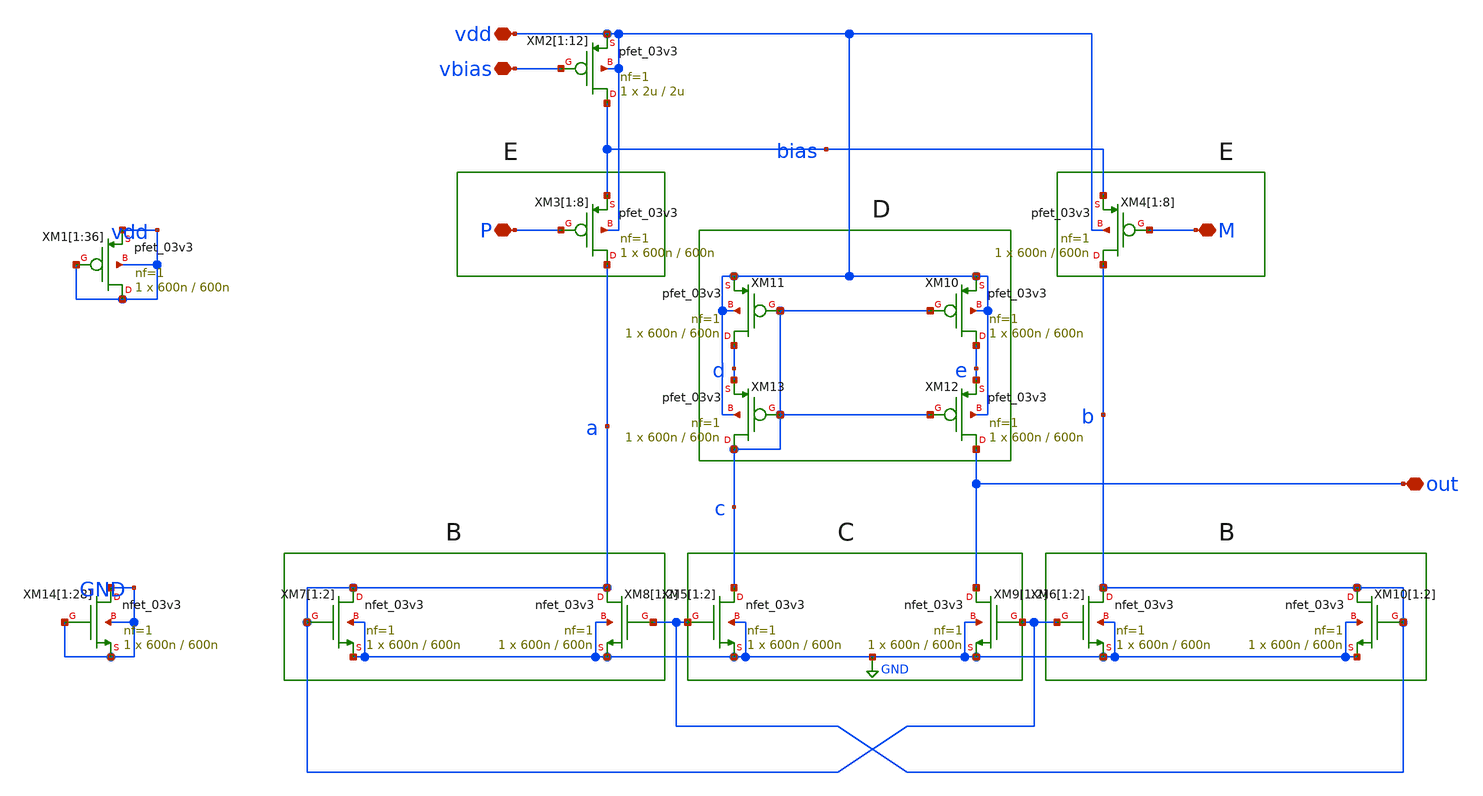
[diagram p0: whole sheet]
** sch_path: Clock_Reference/symbols_clock/comparatornew.sch
**.subckt comparatornew out M P vbias vdd
*.iopin out
*.iopin M
*.iopin P
*.iopin vbias
*.iopin vdd
XM2[1] bias vbias vdd vdd pfet_03v3 L=2u W=2u nf=1 ad='int((nf+1)/2) * W/nf * 0.18u' as='int((nf+2)/2) * W/nf * 0.18u'
+ pd='2*int((nf+1)/2) * (W/nf + 0.18u)' ps='2*int((nf+2)/2) * (W/nf + 0.18u)' nrd='0.18u / W' nrs='0.18u / W'
+ sa=0 sb=0 sd=0 m=1
XM2[2] bias vbias vdd vdd pfet_03v3 L=2u W=2u nf=1 ad='int((nf+1)/2) * W/nf * 0.18u' as='int((nf+2)/2) * W/nf * 0.18u'
+ pd='2*int((nf+1)/2) * (W/nf + 0.18u)' ps='2*int((nf+2)/2) * (W/nf + 0.18u)' nrd='0.18u / W' nrs='0.18u / W'
+ sa=0 sb=0 sd=0 m=1
XM2[3] bias vbias vdd vdd pfet_03v3 L=2u W=2u nf=1 ad='int((nf+1)/2) * W/nf * 0.18u' as='int((nf+2)/2) * W/nf * 0.18u'
+ pd='2*int((nf+1)/2) * (W/nf + 0.18u)' ps='2*int((nf+2)/2) * (W/nf + 0.18u)' nrd='0.18u / W' nrs='0.18u / W'
+ sa=0 sb=0 sd=0 m=1
XM2[4] bias vbias vdd vdd pfet_03v3 L=2u W=2u nf=1 ad='int((nf+1)/2) * W/nf * 0.18u' as='int((nf+2)/2) * W/nf * 0.18u'
+ pd='2*int((nf+1)/2) * (W/nf + 0.18u)' ps='2*int((nf+2)/2) * (W/nf + 0.18u)' nrd='0.18u / W' nrs='0.18u / W'
+ sa=0 sb=0 sd=0 m=1
XM2[5] bias vbias vdd vdd pfet_03v3 L=2u W=2u nf=1 ad='int((nf+1)/2) * W/nf * 0.18u' as='int((nf+2)/2) * W/nf * 0.18u'
+ pd='2*int((nf+1)/2) * (W/nf + 0.18u)' ps='2*int((nf+2)/2) * (W/nf + 0.18u)' nrd='0.18u / W' nrs='0.18u / W'
+ sa=0 sb=0 sd=0 m=1
XM2[6] bias vbias vdd vdd pfet_03v3 L=2u W=2u nf=1 ad='int((nf+1)/2) * W/nf * 0.18u' as='int((nf+2)/2) * W/nf * 0.18u'
+ pd='2*int((nf+1)/2) * (W/nf + 0.18u)' ps='2*int((nf+2)/2) * (W/nf + 0.18u)' nrd='0.18u / W' nrs='0.18u / W'
+ sa=0 sb=0 sd=0 m=1
XM2[7] bias vbias vdd vdd pfet_03v3 L=2u W=2u nf=1 ad='int((nf+1)/2) * W/nf * 0.18u' as='int((nf+2)/2) * W/nf * 0.18u'
+ pd='2*int((nf+1)/2) * (W/nf + 0.18u)' ps='2*int((nf+2)/2) * (W/nf + 0.18u)' nrd='0.18u / W' nrs='0.18u / W'
+ sa=0 sb=0 sd=0 m=1
XM2[8] bias vbias vdd vdd pfet_03v3 L=2u W=2u nf=1 ad='int((nf+1)/2) * W/nf * 0.18u' as='int((nf+2)/2) * W/nf * 0.18u'
+ pd='2*int((nf+1)/2) * (W/nf + 0.18u)' ps='2*int((nf+2)/2) * (W/nf + 0.18u)' nrd='0.18u / W' nrs='0.18u / W'
+ sa=0 sb=0 sd=0 m=1
XM2[9] bias vbias vdd vdd pfet_03v3 L=2u W=2u nf=1 ad='int((nf+1)/2) * W/nf * 0.18u' as='int((nf+2)/2) * W/nf * 0.18u'
+ pd='2*int((nf+1)/2) * (W/nf + 0.18u)' ps='2*int((nf+2)/2) * (W/nf + 0.18u)' nrd='0.18u / W' nrs='0.18u / W'
+ sa=0 sb=0 sd=0 m=1
XM2[10] bias vbias vdd vdd pfet_03v3 L=2u W=2u nf=1 ad='int((nf+1)/2) * W/nf * 0.18u' as='int((nf+2)/2) * W/nf * 0.18u'
+ pd='2*int((nf+1)/2) * (W/nf + 0.18u)' ps='2*int((nf+2)/2) * (W/nf + 0.18u)' nrd='0.18u / W' nrs='0.18u / W'
+ sa=0 sb=0 sd=0 m=1
XM2[11] bias vbias vdd vdd pfet_03v3 L=2u W=2u nf=1 ad='int((nf+1)/2) * W/nf * 0.18u' as='int((nf+2)/2) * W/nf * 0.18u'
+ pd='2*int((nf+1)/2) * (W/nf + 0.18u)' ps='2*int((nf+2)/2) * (W/nf + 0.18u)' nrd='0.18u / W' nrs='0.18u / W'
+ sa=0 sb=0 sd=0 m=1
XM2[12] bias vbias vdd vdd pfet_03v3 L=2u W=2u nf=1 ad='int((nf+1)/2) * W/nf * 0.18u' as='int((nf+2)/2) * W/nf * 0.18u'
+ pd='2*int((nf+1)/2) * (W/nf + 0.18u)' ps='2*int((nf+2)/2) * (W/nf + 0.18u)' nrd='0.18u / W' nrs='0.18u / W'
+ sa=0 sb=0 sd=0 m=1
XM3[1] a P bias vdd pfet_03v3 L=600n W=600n nf=1 ad='int((nf+1)/2) * W/nf * 0.18u' as='int((nf+2)/2) * W/nf * 0.18u'
+ pd='2*int((nf+1)/2) * (W/nf + 0.18u)' ps='2*int((nf+2)/2) * (W/nf + 0.18u)' nrd='0.18u / W' nrs='0.18u / W'
+ sa=0 sb=0 sd=0 m=1
XM3[2] a P bias vdd pfet_03v3 L=600n W=600n nf=1 ad='int((nf+1)/2) * W/nf * 0.18u' as='int((nf+2)/2) * W/nf * 0.18u'
+ pd='2*int((nf+1)/2) * (W/nf + 0.18u)' ps='2*int((nf+2)/2) * (W/nf + 0.18u)' nrd='0.18u / W' nrs='0.18u / W'
+ sa=0 sb=0 sd=0 m=1
XM3[3] a P bias vdd pfet_03v3 L=600n W=600n nf=1 ad='int((nf+1)/2) * W/nf * 0.18u' as='int((nf+2)/2) * W/nf * 0.18u'
+ pd='2*int((nf+1)/2) * (W/nf + 0.18u)' ps='2*int((nf+2)/2) * (W/nf + 0.18u)' nrd='0.18u / W' nrs='0.18u / W'
+ sa=0 sb=0 sd=0 m=1
XM3[4] a P bias vdd pfet_03v3 L=600n W=600n nf=1 ad='int((nf+1)/2) * W/nf * 0.18u' as='int((nf+2)/2) * W/nf * 0.18u'
+ pd='2*int((nf+1)/2) * (W/nf + 0.18u)' ps='2*int((nf+2)/2) * (W/nf + 0.18u)' nrd='0.18u / W' nrs='0.18u / W'
+ sa=0 sb=0 sd=0 m=1
XM3[5] a P bias vdd pfet_03v3 L=600n W=600n nf=1 ad='int((nf+1)/2) * W/nf * 0.18u' as='int((nf+2)/2) * W/nf * 0.18u'
+ pd='2*int((nf+1)/2) * (W/nf + 0.18u)' ps='2*int((nf+2)/2) * (W/nf + 0.18u)' nrd='0.18u / W' nrs='0.18u / W'
+ sa=0 sb=0 sd=0 m=1
XM3[6] a P bias vdd pfet_03v3 L=600n W=600n nf=1 ad='int((nf+1)/2) * W/nf * 0.18u' as='int((nf+2)/2) * W/nf * 0.18u'
+ pd='2*int((nf+1)/2) * (W/nf + 0.18u)' ps='2*int((nf+2)/2) * (W/nf + 0.18u)' nrd='0.18u / W' nrs='0.18u / W'
+ sa=0 sb=0 sd=0 m=1
XM3[7] a P bias vdd pfet_03v3 L=600n W=600n nf=1 ad='int((nf+1)/2) * W/nf * 0.18u' as='int((nf+2)/2) * W/nf * 0.18u'
+ pd='2*int((nf+1)/2) * (W/nf + 0.18u)' ps='2*int((nf+2)/2) * (W/nf + 0.18u)' nrd='0.18u / W' nrs='0.18u / W'
+ sa=0 sb=0 sd=0 m=1
XM3[8] a P bias vdd pfet_03v3 L=600n W=600n nf=1 ad='int((nf+1)/2) * W/nf * 0.18u' as='int((nf+2)/2) * W/nf * 0.18u'
+ pd='2*int((nf+1)/2) * (W/nf + 0.18u)' ps='2*int((nf+2)/2) * (W/nf + 0.18u)' nrd='0.18u / W' nrs='0.18u / W'
+ sa=0 sb=0 sd=0 m=1
XM4[1] b M bias vdd pfet_03v3 L=600n W=600n nf=1 ad='int((nf+1)/2) * W/nf * 0.18u' as='int((nf+2)/2) * W/nf * 0.18u'
+ pd='2*int((nf+1)/2) * (W/nf + 0.18u)' ps='2*int((nf+2)/2) * (W/nf + 0.18u)' nrd='0.18u / W' nrs='0.18u / W'
+ sa=0 sb=0 sd=0 m=1
XM4[2] b M bias vdd pfet_03v3 L=600n W=600n nf=1 ad='int((nf+1)/2) * W/nf * 0.18u' as='int((nf+2)/2) * W/nf * 0.18u'
+ pd='2*int((nf+1)/2) * (W/nf + 0.18u)' ps='2*int((nf+2)/2) * (W/nf + 0.18u)' nrd='0.18u / W' nrs='0.18u / W'
+ sa=0 sb=0 sd=0 m=1
XM4[3] b M bias vdd pfet_03v3 L=600n W=600n nf=1 ad='int((nf+1)/2) * W/nf * 0.18u' as='int((nf+2)/2) * W/nf * 0.18u'
+ pd='2*int((nf+1)/2) * (W/nf + 0.18u)' ps='2*int((nf+2)/2) * (W/nf + 0.18u)' nrd='0.18u / W' nrs='0.18u / W'
+ sa=0 sb=0 sd=0 m=1
XM4[4] b M bias vdd pfet_03v3 L=600n W=600n nf=1 ad='int((nf+1)/2) * W/nf * 0.18u' as='int((nf+2)/2) * W/nf * 0.18u'
+ pd='2*int((nf+1)/2) * (W/nf + 0.18u)' ps='2*int((nf+2)/2) * (W/nf + 0.18u)' nrd='0.18u / W' nrs='0.18u / W'
+ sa=0 sb=0 sd=0 m=1
XM4[5] b M bias vdd pfet_03v3 L=600n W=600n nf=1 ad='int((nf+1)/2) * W/nf * 0.18u' as='int((nf+2)/2) * W/nf * 0.18u'
+ pd='2*int((nf+1)/2) * (W/nf + 0.18u)' ps='2*int((nf+2)/2) * (W/nf + 0.18u)' nrd='0.18u / W' nrs='0.18u / W'
+ sa=0 sb=0 sd=0 m=1
XM4[6] b M bias vdd pfet_03v3 L=600n W=600n nf=1 ad='int((nf+1)/2) * W/nf * 0.18u' as='int((nf+2)/2) * W/nf * 0.18u'
+ pd='2*int((nf+1)/2) * (W/nf + 0.18u)' ps='2*int((nf+2)/2) * (W/nf + 0.18u)' nrd='0.18u / W' nrs='0.18u / W'
+ sa=0 sb=0 sd=0 m=1
XM4[7] b M bias vdd pfet_03v3 L=600n W=600n nf=1 ad='int((nf+1)/2) * W/nf * 0.18u' as='int((nf+2)/2) * W/nf * 0.18u'
+ pd='2*int((nf+1)/2) * (W/nf + 0.18u)' ps='2*int((nf+2)/2) * (W/nf + 0.18u)' nrd='0.18u / W' nrs='0.18u / W'
+ sa=0 sb=0 sd=0 m=1
XM4[8] b M bias vdd pfet_03v3 L=600n W=600n nf=1 ad='int((nf+1)/2) * W/nf * 0.18u' as='int((nf+2)/2) * W/nf * 0.18u'
+ pd='2*int((nf+1)/2) * (W/nf + 0.18u)' ps='2*int((nf+2)/2) * (W/nf + 0.18u)' nrd='0.18u / W' nrs='0.18u / W'
+ sa=0 sb=0 sd=0 m=1
XM6[1] b a GND GND nfet_03v3 L=600n W=600n nf=1 ad='int((nf+1)/2) * W/nf * 0.18u' as='int((nf+2)/2) * W/nf * 0.18u'
+ pd='2*int((nf+1)/2) * (W/nf + 0.18u)' ps='2*int((nf+2)/2) * (W/nf + 0.18u)' nrd='0.18u / W' nrs='0.18u / W'
+ sa=0 sb=0 sd=0 m=1
XM6[2] b a GND GND nfet_03v3 L=600n W=600n nf=1 ad='int((nf+1)/2) * W/nf * 0.18u' as='int((nf+2)/2) * W/nf * 0.18u'
+ pd='2*int((nf+1)/2) * (W/nf + 0.18u)' ps='2*int((nf+2)/2) * (W/nf + 0.18u)' nrd='0.18u / W' nrs='0.18u / W'
+ sa=0 sb=0 sd=0 m=1
XM5[1] c b GND GND nfet_03v3 L=600n W=600n nf=1 ad='int((nf+1)/2) * W/nf * 0.18u' as='int((nf+2)/2) * W/nf * 0.18u'
+ pd='2*int((nf+1)/2) * (W/nf + 0.18u)' ps='2*int((nf+2)/2) * (W/nf + 0.18u)' nrd='0.18u / W' nrs='0.18u / W'
+ sa=0 sb=0 sd=0 m=1
XM5[2] c b GND GND nfet_03v3 L=600n W=600n nf=1 ad='int((nf+1)/2) * W/nf * 0.18u' as='int((nf+2)/2) * W/nf * 0.18u'
+ pd='2*int((nf+1)/2) * (W/nf + 0.18u)' ps='2*int((nf+2)/2) * (W/nf + 0.18u)' nrd='0.18u / W' nrs='0.18u / W'
+ sa=0 sb=0 sd=0 m=1
XM7[1] a a GND GND nfet_03v3 L=600n W=600n nf=1 ad='int((nf+1)/2) * W/nf * 0.18u' as='int((nf+2)/2) * W/nf * 0.18u'
+ pd='2*int((nf+1)/2) * (W/nf + 0.18u)' ps='2*int((nf+2)/2) * (W/nf + 0.18u)' nrd='0.18u / W' nrs='0.18u / W'
+ sa=0 sb=0 sd=0 m=1
XM7[2] a a GND GND nfet_03v3 L=600n W=600n nf=1 ad='int((nf+1)/2) * W/nf * 0.18u' as='int((nf+2)/2) * W/nf * 0.18u'
+ pd='2*int((nf+1)/2) * (W/nf + 0.18u)' ps='2*int((nf+2)/2) * (W/nf + 0.18u)' nrd='0.18u / W' nrs='0.18u / W'
+ sa=0 sb=0 sd=0 m=1
XM8[1] a b GND GND nfet_03v3 L=600n W=600n nf=1 ad='int((nf+1)/2) * W/nf * 0.18u' as='int((nf+2)/2) * W/nf * 0.18u'
+ pd='2*int((nf+1)/2) * (W/nf + 0.18u)' ps='2*int((nf+2)/2) * (W/nf + 0.18u)' nrd='0.18u / W' nrs='0.18u / W'
+ sa=0 sb=0 sd=0 m=1
XM8[2] a b GND GND nfet_03v3 L=600n W=600n nf=1 ad='int((nf+1)/2) * W/nf * 0.18u' as='int((nf+2)/2) * W/nf * 0.18u'
+ pd='2*int((nf+1)/2) * (W/nf + 0.18u)' ps='2*int((nf+2)/2) * (W/nf + 0.18u)' nrd='0.18u / W' nrs='0.18u / W'
+ sa=0 sb=0 sd=0 m=1
XM9[1] out a GND GND nfet_03v3 L=600n W=600n nf=1 ad='int((nf+1)/2) * W/nf * 0.18u' as='int((nf+2)/2) * W/nf * 0.18u'
+ pd='2*int((nf+1)/2) * (W/nf + 0.18u)' ps='2*int((nf+2)/2) * (W/nf + 0.18u)' nrd='0.18u / W' nrs='0.18u / W'
+ sa=0 sb=0 sd=0 m=1
XM9[2] out a GND GND nfet_03v3 L=600n W=600n nf=1 ad='int((nf+1)/2) * W/nf * 0.18u' as='int((nf+2)/2) * W/nf * 0.18u'
+ pd='2*int((nf+1)/2) * (W/nf + 0.18u)' ps='2*int((nf+2)/2) * (W/nf + 0.18u)' nrd='0.18u / W' nrs='0.18u / W'
+ sa=0 sb=0 sd=0 m=1
XM10[1] b b GND GND nfet_03v3 L=600n W=600n nf=1 ad='int((nf+1)/2) * W/nf * 0.18u' as='int((nf+2)/2) * W/nf * 0.18u'
+ pd='2*int((nf+1)/2) * (W/nf + 0.18u)' ps='2*int((nf+2)/2) * (W/nf + 0.18u)' nrd='0.18u / W' nrs='0.18u / W'
+ sa=0 sb=0 sd=0 m=1
XM10[2] b b GND GND nfet_03v3 L=600n W=600n nf=1 ad='int((nf+1)/2) * W/nf * 0.18u' as='int((nf+2)/2) * W/nf * 0.18u'
+ pd='2*int((nf+1)/2) * (W/nf + 0.18u)' ps='2*int((nf+2)/2) * (W/nf + 0.18u)' nrd='0.18u / W' nrs='0.18u / W'
+ sa=0 sb=0 sd=0 m=1
XM10 e c vdd vdd pfet_03v3 L=600n W=600n nf=1 ad='int((nf+1)/2) * W/nf * 0.18u' as='int((nf+2)/2) * W/nf * 0.18u'
+ pd='2*int((nf+1)/2) * (W/nf + 0.18u)' ps='2*int((nf+2)/2) * (W/nf + 0.18u)' nrd='0.18u / W' nrs='0.18u / W'
+ sa=0 sb=0 sd=0 m=1
XM11 d c vdd vdd pfet_03v3 L=600n W=600n nf=1 ad='int((nf+1)/2) * W/nf * 0.18u' as='int((nf+2)/2) * W/nf * 0.18u'
+ pd='2*int((nf+1)/2) * (W/nf + 0.18u)' ps='2*int((nf+2)/2) * (W/nf + 0.18u)' nrd='0.18u / W' nrs='0.18u / W'
+ sa=0 sb=0 sd=0 m=1
XM12 out c e vdd pfet_03v3 L=600n W=600n nf=1 ad='int((nf+1)/2) * W/nf * 0.18u' as='int((nf+2)/2) * W/nf * 0.18u'
+ pd='2*int((nf+1)/2) * (W/nf + 0.18u)' ps='2*int((nf+2)/2) * (W/nf + 0.18u)' nrd='0.18u / W' nrs='0.18u / W'
+ sa=0 sb=0 sd=0 m=1
XM13 c c d vdd pfet_03v3 L=600n W=600n nf=1 ad='int((nf+1)/2) * W/nf * 0.18u' as='int((nf+2)/2) * W/nf * 0.18u'
+ pd='2*int((nf+1)/2) * (W/nf + 0.18u)' ps='2*int((nf+2)/2) * (W/nf + 0.18u)' nrd='0.18u / W' nrs='0.18u / W'
+ sa=0 sb=0 sd=0 m=1
XM14[1] GND GND GND GND nfet_03v3 L=600n W=600n nf=1 ad='int((nf+1)/2) * W/nf * 0.18u' as='int((nf+2)/2) * W/nf * 0.18u'
+ pd='2*int((nf+1)/2) * (W/nf + 0.18u)' ps='2*int((nf+2)/2) * (W/nf + 0.18u)' nrd='0.18u / W' nrs='0.18u / W'
+ sa=0 sb=0 sd=0 m=1
XM14[2] GND GND GND GND nfet_03v3 L=600n W=600n nf=1 ad='int((nf+1)/2) * W/nf * 0.18u' as='int((nf+2)/2) * W/nf * 0.18u'
+ pd='2*int((nf+1)/2) * (W/nf + 0.18u)' ps='2*int((nf+2)/2) * (W/nf + 0.18u)' nrd='0.18u / W' nrs='0.18u / W'
+ sa=0 sb=0 sd=0 m=1
XM14[3] GND GND GND GND nfet_03v3 L=600n W=600n nf=1 ad='int((nf+1)/2) * W/nf * 0.18u' as='int((nf+2)/2) * W/nf * 0.18u'
+ pd='2*int((nf+1)/2) * (W/nf + 0.18u)' ps='2*int((nf+2)/2) * (W/nf + 0.18u)' nrd='0.18u / W' nrs='0.18u / W'
+ sa=0 sb=0 sd=0 m=1
XM14[4] GND GND GND GND nfet_03v3 L=600n W=600n nf=1 ad='int((nf+1)/2) * W/nf * 0.18u' as='int((nf+2)/2) * W/nf * 0.18u'
+ pd='2*int((nf+1)/2) * (W/nf + 0.18u)' ps='2*int((nf+2)/2) * (W/nf + 0.18u)' nrd='0.18u / W' nrs='0.18u / W'
+ sa=0 sb=0 sd=0 m=1
XM14[5] GND GND GND GND nfet_03v3 L=600n W=600n nf=1 ad='int((nf+1)/2) * W/nf * 0.18u' as='int((nf+2)/2) * W/nf * 0.18u'
+ pd='2*int((nf+1)/2) * (W/nf + 0.18u)' ps='2*int((nf+2)/2) * (W/nf + 0.18u)' nrd='0.18u / W' nrs='0.18u / W'
+ sa=0 sb=0 sd=0 m=1
XM14[6] GND GND GND GND nfet_03v3 L=600n W=600n nf=1 ad='int((nf+1)/2) * W/nf * 0.18u' as='int((nf+2)/2) * W/nf * 0.18u'
+ pd='2*int((nf+1)/2) * (W/nf + 0.18u)' ps='2*int((nf+2)/2) * (W/nf + 0.18u)' nrd='0.18u / W' nrs='0.18u / W'
+ sa=0 sb=0 sd=0 m=1
XM14[7] GND GND GND GND nfet_03v3 L=600n W=600n nf=1 ad='int((nf+1)/2) * W/nf * 0.18u' as='int((nf+2)/2) * W/nf * 0.18u'
+ pd='2*int((nf+1)/2) * (W/nf + 0.18u)' ps='2*int((nf+2)/2) * (W/nf + 0.18u)' nrd='0.18u / W' nrs='0.18u / W'
+ sa=0 sb=0 sd=0 m=1
XM14[8] GND GND GND GND nfet_03v3 L=600n W=600n nf=1 ad='int((nf+1)/2) * W/nf * 0.18u' as='int((nf+2)/2) * W/nf * 0.18u'
+ pd='2*int((nf+1)/2) * (W/nf + 0.18u)' ps='2*int((nf+2)/2) * (W/nf + 0.18u)' nrd='0.18u / W' nrs='0.18u / W'
+ sa=0 sb=0 sd=0 m=1
XM14[9] GND GND GND GND nfet_03v3 L=600n W=600n nf=1 ad='int((nf+1)/2) * W/nf * 0.18u' as='int((nf+2)/2) * W/nf * 0.18u'
+ pd='2*int((nf+1)/2) * (W/nf + 0.18u)' ps='2*int((nf+2)/2) * (W/nf + 0.18u)' nrd='0.18u / W' nrs='0.18u / W'
+ sa=0 sb=0 sd=0 m=1
XM14[10] GND GND GND GND nfet_03v3 L=600n W=600n nf=1 ad='int((nf+1)/2) * W/nf * 0.18u' as='int((nf+2)/2) * W/nf * 0.18u'
+ pd='2*int((nf+1)/2) * (W/nf + 0.18u)' ps='2*int((nf+2)/2) * (W/nf + 0.18u)' nrd='0.18u / W' nrs='0.18u / W'
+ sa=0 sb=0 sd=0 m=1
XM14[11] GND GND GND GND nfet_03v3 L=600n W=600n nf=1 ad='int((nf+1)/2) * W/nf * 0.18u' as='int((nf+2)/2) * W/nf * 0.18u'
+ pd='2*int((nf+1)/2) * (W/nf + 0.18u)' ps='2*int((nf+2)/2) * (W/nf + 0.18u)' nrd='0.18u / W' nrs='0.18u / W'
+ sa=0 sb=0 sd=0 m=1
XM14[12] GND GND GND GND nfet_03v3 L=600n W=600n nf=1 ad='int((nf+1)/2) * W/nf * 0.18u' as='int((nf+2)/2) * W/nf * 0.18u'
+ pd='2*int((nf+1)/2) * (W/nf + 0.18u)' ps='2*int((nf+2)/2) * (W/nf + 0.18u)' nrd='0.18u / W' nrs='0.18u / W'
+ sa=0 sb=0 sd=0 m=1
XM14[13] GND GND GND GND nfet_03v3 L=600n W=600n nf=1 ad='int((nf+1)/2) * W/nf * 0.18u' as='int((nf+2)/2) * W/nf * 0.18u'
+ pd='2*int((nf+1)/2) * (W/nf + 0.18u)' ps='2*int((nf+2)/2) * (W/nf + 0.18u)' nrd='0.18u / W' nrs='0.18u / W'
+ sa=0 sb=0 sd=0 m=1
XM14[14] GND GND GND GND nfet_03v3 L=600n W=600n nf=1 ad='int((nf+1)/2) * W/nf * 0.18u' as='int((nf+2)/2) * W/nf * 0.18u'
+ pd='2*int((nf+1)/2) * (W/nf + 0.18u)' ps='2*int((nf+2)/2) * (W/nf + 0.18u)' nrd='0.18u / W' nrs='0.18u / W'
+ sa=0 sb=0 sd=0 m=1
XM14[15] GND GND GND GND nfet_03v3 L=600n W=600n nf=1 ad='int((nf+1)/2) * W/nf * 0.18u' as='int((nf+2)/2) * W/nf * 0.18u'
+ pd='2*int((nf+1)/2) * (W/nf + 0.18u)' ps='2*int((nf+2)/2) * (W/nf + 0.18u)' nrd='0.18u / W' nrs='0.18u / W'
+ sa=0 sb=0 sd=0 m=1
XM14[16] GND GND GND GND nfet_03v3 L=600n W=600n nf=1 ad='int((nf+1)/2) * W/nf * 0.18u' as='int((nf+2)/2) * W/nf * 0.18u'
+ pd='2*int((nf+1)/2) * (W/nf + 0.18u)' ps='2*int((nf+2)/2) * (W/nf + 0.18u)' nrd='0.18u / W' nrs='0.18u / W'
+ sa=0 sb=0 sd=0 m=1
XM14[17] GND GND GND GND nfet_03v3 L=600n W=600n nf=1 ad='int((nf+1)/2) * W/nf * 0.18u' as='int((nf+2)/2) * W/nf * 0.18u'
+ pd='2*int((nf+1)/2) * (W/nf + 0.18u)' ps='2*int((nf+2)/2) * (W/nf + 0.18u)' nrd='0.18u / W' nrs='0.18u / W'
+ sa=0 sb=0 sd=0 m=1
XM14[18] GND GND GND GND nfet_03v3 L=600n W=600n nf=1 ad='int((nf+1)/2) * W/nf * 0.18u' as='int((nf+2)/2) * W/nf * 0.18u'
+ pd='2*int((nf+1)/2) * (W/nf + 0.18u)' ps='2*int((nf+2)/2) * (W/nf + 0.18u)' nrd='0.18u / W' nrs='0.18u / W'
+ sa=0 sb=0 sd=0 m=1
XM14[19] GND GND GND GND nfet_03v3 L=600n W=600n nf=1 ad='int((nf+1)/2) * W/nf * 0.18u' as='int((nf+2)/2) * W/nf * 0.18u'
+ pd='2*int((nf+1)/2) * (W/nf + 0.18u)' ps='2*int((nf+2)/2) * (W/nf + 0.18u)' nrd='0.18u / W' nrs='0.18u / W'
+ sa=0 sb=0 sd=0 m=1
XM14[20] GND GND GND GND nfet_03v3 L=600n W=600n nf=1 ad='int((nf+1)/2) * W/nf * 0.18u' as='int((nf+2)/2) * W/nf * 0.18u'
+ pd='2*int((nf+1)/2) * (W/nf + 0.18u)' ps='2*int((nf+2)/2) * (W/nf + 0.18u)' nrd='0.18u / W' nrs='0.18u / W'
+ sa=0 sb=0 sd=0 m=1
XM14[21] GND GND GND GND nfet_03v3 L=600n W=600n nf=1 ad='int((nf+1)/2) * W/nf * 0.18u' as='int((nf+2)/2) * W/nf * 0.18u'
+ pd='2*int((nf+1)/2) * (W/nf + 0.18u)' ps='2*int((nf+2)/2) * (W/nf + 0.18u)' nrd='0.18u / W' nrs='0.18u / W'
+ sa=0 sb=0 sd=0 m=1
XM14[22] GND GND GND GND nfet_03v3 L=600n W=600n nf=1 ad='int((nf+1)/2) * W/nf * 0.18u' as='int((nf+2)/2) * W/nf * 0.18u'
+ pd='2*int((nf+1)/2) * (W/nf + 0.18u)' ps='2*int((nf+2)/2) * (W/nf + 0.18u)' nrd='0.18u / W' nrs='0.18u / W'
+ sa=0 sb=0 sd=0 m=1
XM14[23] GND GND GND GND nfet_03v3 L=600n W=600n nf=1 ad='int((nf+1)/2) * W/nf * 0.18u' as='int((nf+2)/2) * W/nf * 0.18u'
+ pd='2*int((nf+1)/2) * (W/nf + 0.18u)' ps='2*int((nf+2)/2) * (W/nf + 0.18u)' nrd='0.18u / W' nrs='0.18u / W'
+ sa=0 sb=0 sd=0 m=1
XM14[24] GND GND GND GND nfet_03v3 L=600n W=600n nf=1 ad='int((nf+1)/2) * W/nf * 0.18u' as='int((nf+2)/2) * W/nf * 0.18u'
+ pd='2*int((nf+1)/2) * (W/nf + 0.18u)' ps='2*int((nf+2)/2) * (W/nf + 0.18u)' nrd='0.18u / W' nrs='0.18u / W'
+ sa=0 sb=0 sd=0 m=1
XM14[25] GND GND GND GND nfet_03v3 L=600n W=600n nf=1 ad='int((nf+1)/2) * W/nf * 0.18u' as='int((nf+2)/2) * W/nf * 0.18u'
+ pd='2*int((nf+1)/2) * (W/nf + 0.18u)' ps='2*int((nf+2)/2) * (W/nf + 0.18u)' nrd='0.18u / W' nrs='0.18u / W'
+ sa=0 sb=0 sd=0 m=1
XM14[26] GND GND GND GND nfet_03v3 L=600n W=600n nf=1 ad='int((nf+1)/2) * W/nf * 0.18u' as='int((nf+2)/2) * W/nf * 0.18u'
+ pd='2*int((nf+1)/2) * (W/nf + 0.18u)' ps='2*int((nf+2)/2) * (W/nf + 0.18u)' nrd='0.18u / W' nrs='0.18u / W'
+ sa=0 sb=0 sd=0 m=1
XM14[27] GND GND GND GND nfet_03v3 L=600n W=600n nf=1 ad='int((nf+1)/2) * W/nf * 0.18u' as='int((nf+2)/2) * W/nf * 0.18u'
+ pd='2*int((nf+1)/2) * (W/nf + 0.18u)' ps='2*int((nf+2)/2) * (W/nf + 0.18u)' nrd='0.18u / W' nrs='0.18u / W'
+ sa=0 sb=0 sd=0 m=1
XM14[28] GND GND GND GND nfet_03v3 L=600n W=600n nf=1 ad='int((nf+1)/2) * W/nf * 0.18u' as='int((nf+2)/2) * W/nf * 0.18u'
+ pd='2*int((nf+1)/2) * (W/nf + 0.18u)' ps='2*int((nf+2)/2) * (W/nf + 0.18u)' nrd='0.18u / W' nrs='0.18u / W'
+ sa=0 sb=0 sd=0 m=1
XM1[1] vdd vdd vdd vdd pfet_03v3 L=600n W=600n nf=1 ad='int((nf+1)/2) * W/nf * 0.18u' as='int((nf+2)/2) * W/nf * 0.18u'
+ pd='2*int((nf+1)/2) * (W/nf + 0.18u)' ps='2*int((nf+2)/2) * (W/nf + 0.18u)' nrd='0.18u / W' nrs='0.18u / W'
+ sa=0 sb=0 sd=0 m=1
XM1[2] vdd vdd vdd vdd pfet_03v3 L=600n W=600n nf=1 ad='int((nf+1)/2) * W/nf * 0.18u' as='int((nf+2)/2) * W/nf * 0.18u'
+ pd='2*int((nf+1)/2) * (W/nf + 0.18u)' ps='2*int((nf+2)/2) * (W/nf + 0.18u)' nrd='0.18u / W' nrs='0.18u / W'
+ sa=0 sb=0 sd=0 m=1
XM1[3] vdd vdd vdd vdd pfet_03v3 L=600n W=600n nf=1 ad='int((nf+1)/2) * W/nf * 0.18u' as='int((nf+2)/2) * W/nf * 0.18u'
+ pd='2*int((nf+1)/2) * (W/nf + 0.18u)' ps='2*int((nf+2)/2) * (W/nf + 0.18u)' nrd='0.18u / W' nrs='0.18u / W'
+ sa=0 sb=0 sd=0 m=1
XM1[4] vdd vdd vdd vdd pfet_03v3 L=600n W=600n nf=1 ad='int((nf+1)/2) * W/nf * 0.18u' as='int((nf+2)/2) * W/nf * 0.18u'
+ pd='2*int((nf+1)/2) * (W/nf + 0.18u)' ps='2*int((nf+2)/2) * (W/nf + 0.18u)' nrd='0.18u / W' nrs='0.18u / W'
+ sa=0 sb=0 sd=0 m=1
XM1[5] vdd vdd vdd vdd pfet_03v3 L=600n W=600n nf=1 ad='int((nf+1)/2) * W/nf * 0.18u' as='int((nf+2)/2) * W/nf * 0.18u'
+ pd='2*int((nf+1)/2) * (W/nf + 0.18u)' ps='2*int((nf+2)/2) * (W/nf + 0.18u)' nrd='0.18u / W' nrs='0.18u / W'
+ sa=0 sb=0 sd=0 m=1
XM1[6] vdd vdd vdd vdd pfet_03v3 L=600n W=600n nf=1 ad='int((nf+1)/2) * W/nf * 0.18u' as='int((nf+2)/2) * W/nf * 0.18u'
+ pd='2*int((nf+1)/2) * (W/nf + 0.18u)' ps='2*int((nf+2)/2) * (W/nf + 0.18u)' nrd='0.18u / W' nrs='0.18u / W'
+ sa=0 sb=0 sd=0 m=1
XM1[7] vdd vdd vdd vdd pfet_03v3 L=600n W=600n nf=1 ad='int((nf+1)/2) * W/nf * 0.18u' as='int((nf+2)/2) * W/nf * 0.18u'
+ pd='2*int((nf+1)/2) * (W/nf + 0.18u)' ps='2*int((nf+2)/2) * (W/nf + 0.18u)' nrd='0.18u / W' nrs='0.18u / W'
+ sa=0 sb=0 sd=0 m=1
XM1[8] vdd vdd vdd vdd pfet_03v3 L=600n W=600n nf=1 ad='int((nf+1)/2) * W/nf * 0.18u' as='int((nf+2)/2) * W/nf * 0.18u'
+ pd='2*int((nf+1)/2) * (W/nf + 0.18u)' ps='2*int((nf+2)/2) * (W/nf + 0.18u)' nrd='0.18u / W' nrs='0.18u / W'
+ sa=0 sb=0 sd=0 m=1
XM1[9] vdd vdd vdd vdd pfet_03v3 L=600n W=600n nf=1 ad='int((nf+1)/2) * W/nf * 0.18u' as='int((nf+2)/2) * W/nf * 0.18u'
+ pd='2*int((nf+1)/2) * (W/nf + 0.18u)' ps='2*int((nf+2)/2) * (W/nf + 0.18u)' nrd='0.18u / W' nrs='0.18u / W'
+ sa=0 sb=0 sd=0 m=1
XM1[10] vdd vdd vdd vdd pfet_03v3 L=600n W=600n nf=1 ad='int((nf+1)/2) * W/nf * 0.18u' as='int((nf+2)/2) * W/nf * 0.18u'
+ pd='2*int((nf+1)/2) * (W/nf + 0.18u)' ps='2*int((nf+2)/2) * (W/nf + 0.18u)' nrd='0.18u / W' nrs='0.18u / W'
+ sa=0 sb=0 sd=0 m=1
XM1[11] vdd vdd vdd vdd pfet_03v3 L=600n W=600n nf=1 ad='int((nf+1)/2) * W/nf * 0.18u' as='int((nf+2)/2) * W/nf * 0.18u'
+ pd='2*int((nf+1)/2) * (W/nf + 0.18u)' ps='2*int((nf+2)/2) * (W/nf + 0.18u)' nrd='0.18u / W' nrs='0.18u / W'
+ sa=0 sb=0 sd=0 m=1
XM1[12] vdd vdd vdd vdd pfet_03v3 L=600n W=600n nf=1 ad='int((nf+1)/2) * W/nf * 0.18u' as='int((nf+2)/2) * W/nf * 0.18u'
+ pd='2*int((nf+1)/2) * (W/nf + 0.18u)' ps='2*int((nf+2)/2) * (W/nf + 0.18u)' nrd='0.18u / W' nrs='0.18u / W'
+ sa=0 sb=0 sd=0 m=1
XM1[13] vdd vdd vdd vdd pfet_03v3 L=600n W=600n nf=1 ad='int((nf+1)/2) * W/nf * 0.18u' as='int((nf+2)/2) * W/nf * 0.18u'
+ pd='2*int((nf+1)/2) * (W/nf + 0.18u)' ps='2*int((nf+2)/2) * (W/nf + 0.18u)' nrd='0.18u / W' nrs='0.18u / W'
+ sa=0 sb=0 sd=0 m=1
XM1[14] vdd vdd vdd vdd pfet_03v3 L=600n W=600n nf=1 ad='int((nf+1)/2) * W/nf * 0.18u' as='int((nf+2)/2) * W/nf * 0.18u'
+ pd='2*int((nf+1)/2) * (W/nf + 0.18u)' ps='2*int((nf+2)/2) * (W/nf + 0.18u)' nrd='0.18u / W' nrs='0.18u / W'
+ sa=0 sb=0 sd=0 m=1
XM1[15] vdd vdd vdd vdd pfet_03v3 L=600n W=600n nf=1 ad='int((nf+1)/2) * W/nf * 0.18u' as='int((nf+2)/2) * W/nf * 0.18u'
+ pd='2*int((nf+1)/2) * (W/nf + 0.18u)' ps='2*int((nf+2)/2) * (W/nf + 0.18u)' nrd='0.18u / W' nrs='0.18u / W'
+ sa=0 sb=0 sd=0 m=1
XM1[16] vdd vdd vdd vdd pfet_03v3 L=600n W=600n nf=1 ad='int((nf+1)/2) * W/nf * 0.18u' as='int((nf+2)/2) * W/nf * 0.18u'
+ pd='2*int((nf+1)/2) * (W/nf + 0.18u)' ps='2*int((nf+2)/2) * (W/nf + 0.18u)' nrd='0.18u / W' nrs='0.18u / W'
+ sa=0 sb=0 sd=0 m=1
XM1[17] vdd vdd vdd vdd pfet_03v3 L=600n W=600n nf=1 ad='int((nf+1)/2) * W/nf * 0.18u' as='int((nf+2)/2) * W/nf * 0.18u'
+ pd='2*int((nf+1)/2) * (W/nf + 0.18u)' ps='2*int((nf+2)/2) * (W/nf + 0.18u)' nrd='0.18u / W' nrs='0.18u / W'
+ sa=0 sb=0 sd=0 m=1
XM1[18] vdd vdd vdd vdd pfet_03v3 L=600n W=600n nf=1 ad='int((nf+1)/2) * W/nf * 0.18u' as='int((nf+2)/2) * W/nf * 0.18u'
+ pd='2*int((nf+1)/2) * (W/nf + 0.18u)' ps='2*int((nf+2)/2) * (W/nf + 0.18u)' nrd='0.18u / W' nrs='0.18u / W'
+ sa=0 sb=0 sd=0 m=1
XM1[19] vdd vdd vdd vdd pfet_03v3 L=600n W=600n nf=1 ad='int((nf+1)/2) * W/nf * 0.18u' as='int((nf+2)/2) * W/nf * 0.18u'
+ pd='2*int((nf+1)/2) * (W/nf + 0.18u)' ps='2*int((nf+2)/2) * (W/nf + 0.18u)' nrd='0.18u / W' nrs='0.18u / W'
+ sa=0 sb=0 sd=0 m=1
XM1[20] vdd vdd vdd vdd pfet_03v3 L=600n W=600n nf=1 ad='int((nf+1)/2) * W/nf * 0.18u' as='int((nf+2)/2) * W/nf * 0.18u'
+ pd='2*int((nf+1)/2) * (W/nf + 0.18u)' ps='2*int((nf+2)/2) * (W/nf + 0.18u)' nrd='0.18u / W' nrs='0.18u / W'
+ sa=0 sb=0 sd=0 m=1
XM1[21] vdd vdd vdd vdd pfet_03v3 L=600n W=600n nf=1 ad='int((nf+1)/2) * W/nf * 0.18u' as='int((nf+2)/2) * W/nf * 0.18u'
+ pd='2*int((nf+1)/2) * (W/nf + 0.18u)' ps='2*int((nf+2)/2) * (W/nf + 0.18u)' nrd='0.18u / W' nrs='0.18u / W'
+ sa=0 sb=0 sd=0 m=1
XM1[22] vdd vdd vdd vdd pfet_03v3 L=600n W=600n nf=1 ad='int((nf+1)/2) * W/nf * 0.18u' as='int((nf+2)/2) * W/nf * 0.18u'
+ pd='2*int((nf+1)/2) * (W/nf + 0.18u)' ps='2*int((nf+2)/2) * (W/nf + 0.18u)' nrd='0.18u / W' nrs='0.18u / W'
+ sa=0 sb=0 sd=0 m=1
XM1[23] vdd vdd vdd vdd pfet_03v3 L=600n W=600n nf=1 ad='int((nf+1)/2) * W/nf * 0.18u' as='int((nf+2)/2) * W/nf * 0.18u'
+ pd='2*int((nf+1)/2) * (W/nf + 0.18u)' ps='2*int((nf+2)/2) * (W/nf + 0.18u)' nrd='0.18u / W' nrs='0.18u / W'
+ sa=0 sb=0 sd=0 m=1
XM1[24] vdd vdd vdd vdd pfet_03v3 L=600n W=600n nf=1 ad='int((nf+1)/2) * W/nf * 0.18u' as='int((nf+2)/2) * W/nf * 0.18u'
+ pd='2*int((nf+1)/2) * (W/nf + 0.18u)' ps='2*int((nf+2)/2) * (W/nf + 0.18u)' nrd='0.18u / W' nrs='0.18u / W'
+ sa=0 sb=0 sd=0 m=1
XM1[25] vdd vdd vdd vdd pfet_03v3 L=600n W=600n nf=1 ad='int((nf+1)/2) * W/nf * 0.18u' as='int((nf+2)/2) * W/nf * 0.18u'
+ pd='2*int((nf+1)/2) * (W/nf + 0.18u)' ps='2*int((nf+2)/2) * (W/nf + 0.18u)' nrd='0.18u / W' nrs='0.18u / W'
+ sa=0 sb=0 sd=0 m=1
XM1[26] vdd vdd vdd vdd pfet_03v3 L=600n W=600n nf=1 ad='int((nf+1)/2) * W/nf * 0.18u' as='int((nf+2)/2) * W/nf * 0.18u'
+ pd='2*int((nf+1)/2) * (W/nf + 0.18u)' ps='2*int((nf+2)/2) * (W/nf + 0.18u)' nrd='0.18u / W' nrs='0.18u / W'
+ sa=0 sb=0 sd=0 m=1
XM1[27] vdd vdd vdd vdd pfet_03v3 L=600n W=600n nf=1 ad='int((nf+1)/2) * W/nf * 0.18u' as='int((nf+2)/2) * W/nf * 0.18u'
+ pd='2*int((nf+1)/2) * (W/nf + 0.18u)' ps='2*int((nf+2)/2) * (W/nf + 0.18u)' nrd='0.18u / W' nrs='0.18u / W'
+ sa=0 sb=0 sd=0 m=1
XM1[28] vdd vdd vdd vdd pfet_03v3 L=600n W=600n nf=1 ad='int((nf+1)/2) * W/nf * 0.18u' as='int((nf+2)/2) * W/nf * 0.18u'
+ pd='2*int((nf+1)/2) * (W/nf + 0.18u)' ps='2*int((nf+2)/2) * (W/nf + 0.18u)' nrd='0.18u / W' nrs='0.18u / W'
+ sa=0 sb=0 sd=0 m=1
XM1[29] vdd vdd vdd vdd pfet_03v3 L=600n W=600n nf=1 ad='int((nf+1)/2) * W/nf * 0.18u' as='int((nf+2)/2) * W/nf * 0.18u'
+ pd='2*int((nf+1)/2) * (W/nf + 0.18u)' ps='2*int((nf+2)/2) * (W/nf + 0.18u)' nrd='0.18u / W' nrs='0.18u / W'
+ sa=0 sb=0 sd=0 m=1
XM1[30] vdd vdd vdd vdd pfet_03v3 L=600n W=600n nf=1 ad='int((nf+1)/2) * W/nf * 0.18u' as='int((nf+2)/2) * W/nf * 0.18u'
+ pd='2*int((nf+1)/2) * (W/nf + 0.18u)' ps='2*int((nf+2)/2) * (W/nf + 0.18u)' nrd='0.18u / W' nrs='0.18u / W'
+ sa=0 sb=0 sd=0 m=1
XM1[31] vdd vdd vdd vdd pfet_03v3 L=600n W=600n nf=1 ad='int((nf+1)/2) * W/nf * 0.18u' as='int((nf+2)/2) * W/nf * 0.18u'
+ pd='2*int((nf+1)/2) * (W/nf + 0.18u)' ps='2*int((nf+2)/2) * (W/nf + 0.18u)' nrd='0.18u / W' nrs='0.18u / W'
+ sa=0 sb=0 sd=0 m=1
XM1[32] vdd vdd vdd vdd pfet_03v3 L=600n W=600n nf=1 ad='int((nf+1)/2) * W/nf * 0.18u' as='int((nf+2)/2) * W/nf * 0.18u'
+ pd='2*int((nf+1)/2) * (W/nf + 0.18u)' ps='2*int((nf+2)/2) * (W/nf + 0.18u)' nrd='0.18u / W' nrs='0.18u / W'
+ sa=0 sb=0 sd=0 m=1
XM1[33] vdd vdd vdd vdd pfet_03v3 L=600n W=600n nf=1 ad='int((nf+1)/2) * W/nf * 0.18u' as='int((nf+2)/2) * W/nf * 0.18u'
+ pd='2*int((nf+1)/2) * (W/nf + 0.18u)' ps='2*int((nf+2)/2) * (W/nf + 0.18u)' nrd='0.18u / W' nrs='0.18u / W'
+ sa=0 sb=0 sd=0 m=1
XM1[34] vdd vdd vdd vdd pfet_03v3 L=600n W=600n nf=1 ad='int((nf+1)/2) * W/nf * 0.18u' as='int((nf+2)/2) * W/nf * 0.18u'
+ pd='2*int((nf+1)/2) * (W/nf + 0.18u)' ps='2*int((nf+2)/2) * (W/nf + 0.18u)' nrd='0.18u / W' nrs='0.18u / W'
+ sa=0 sb=0 sd=0 m=1
XM1[35] vdd vdd vdd vdd pfet_03v3 L=600n W=600n nf=1 ad='int((nf+1)/2) * W/nf * 0.18u' as='int((nf+2)/2) * W/nf * 0.18u'
+ pd='2*int((nf+1)/2) * (W/nf + 0.18u)' ps='2*int((nf+2)/2) * (W/nf + 0.18u)' nrd='0.18u / W' nrs='0.18u / W'
+ sa=0 sb=0 sd=0 m=1
XM1[36] vdd vdd vdd vdd pfet_03v3 L=600n W=600n nf=1 ad='int((nf+1)/2) * W/nf * 0.18u' as='int((nf+2)/2) * W/nf * 0.18u'
+ pd='2*int((nf+1)/2) * (W/nf + 0.18u)' ps='2*int((nf+2)/2) * (W/nf + 0.18u)' nrd='0.18u / W' nrs='0.18u / W'
+ sa=0 sb=0 sd=0 m=1
**.ends
.GLOBAL GND
.end
